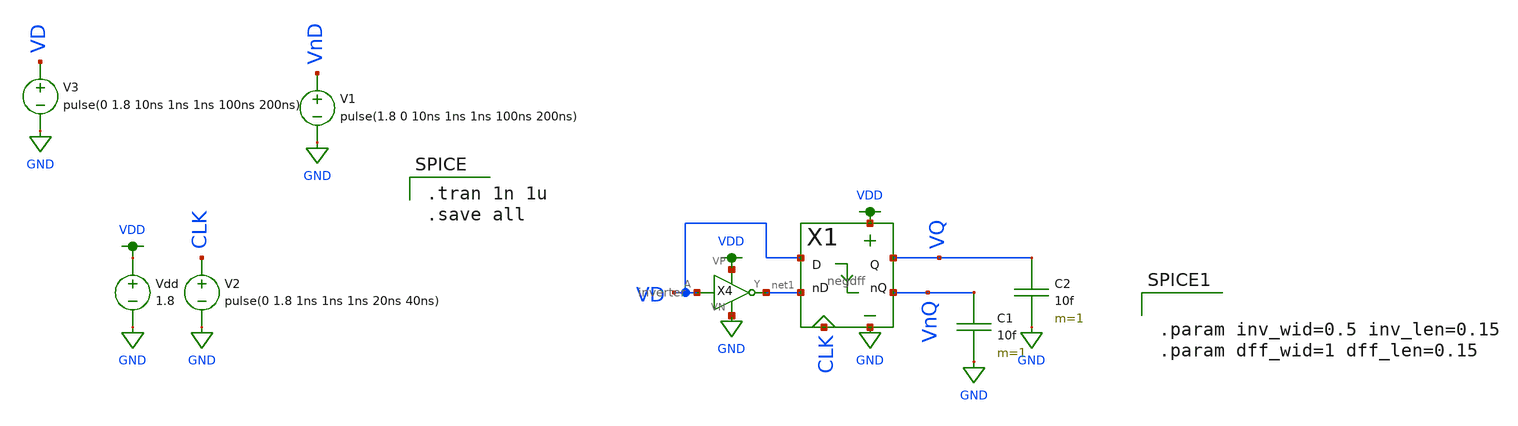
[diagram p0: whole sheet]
** sch_path: test_dff_tt2.sch
**.subckt test_dff_tt2
Vdd VDD GND 1.8
V2 CLK GND pulse(0 1.8 1ns 1ns 1ns 20ns 40ns)
V3 VD GND pulse(0 1.8 10ns 1ns 1ns 100ns 200ns)
V1 VnD GND pulse(1.8 0 10ns 1ns 1ns 100ns 200ns)
X4 VD net1 VDD GND inverter
C1 VnQ GND 10f m=1
C2 VQ GND 10f m=1
X1 GND VDD VnQ VQ CLK net1 VD negdff
**** begin user architecture code

.tran 1n 1u
.save all


.lib $::SKYWATER_MODELS/sky130.lib.spice tt



.param inv_wid=0.5 inv_len=0.15
.param dff_wid=1 dff_len=0.15


**** end user architecture code
**.ends

* expanding   symbol:  inverter.sym # of pins=4
** sym_path: inverter.sym
** sch_path: inverter.sch
.subckt inverter A Y VP VN
*.iopin VP
*.ipin A
*.opin Y
*.iopin VN
XM2 Y A VP VP sky130_fd_pr__pfet_01v8 L={inv_len} W={inv_wid} nf=1 ad='int((nf+1)/2) * W/nf * 0.29' as='int((nf+2)/2) * W/nf * 0.29'
+ pd='2*int((nf+1)/2) * (W/nf + 0.29)' ps='2*int((nf+2)/2) * (W/nf + 0.29)' nrd='0.29 / W' nrs='0.29 / W'
+ sa=0 sb=0 sd=0 mult=1 m=1
XM1 Y A VN VN sky130_fd_pr__nfet_01v8 L={inv_len} W={inv_wid} nf=1 ad='int((nf+1)/2) * W/nf * 0.29' as='int((nf+2)/2) * W/nf * 0.29'
+ pd='2*int((nf+1)/2) * (W/nf + 0.29)' ps='2*int((nf+2)/2) * (W/nf + 0.29)' nrd='0.29 / W' nrs='0.29 / W'
+ sa=0 sb=0 sd=0 mult=1 m=1
.ends


* expanding   symbol:  negdff.sym # of pins=7
** sym_path: negdff.sym
** sch_path: negdff.sch
.subckt negdff VN VP nQ Q PHI nD D
*.iopin VP
*.ipin D
*.opin Q
*.ipin nD
*.ipin PHI
*.opin nQ
*.iopin VN
X1 VN VP nQI QI PHI nD D n_csrl_latch
X2 VN VP nQ Q PHI nQI QI csrl_latch
.ends


* expanding   symbol:  n_csrl_latch.sym # of pins=7
** sym_path: n_csrl_latch.sym
** sch_path: n_csrl_latch.sch
.subckt n_csrl_latch VN VP nQ Q PHI nD D
*.ipin D
*.ipin nD
*.opin nQ
*.opin Q
*.ipin PHI
*.iopin VP
*.iopin VN
XM1 VN nD net3 VN sky130_fd_pr__nfet_01v8 L={dff_len} W={dff_wid} nf=1 ad='int((nf+1)/2) * W/nf * 0.29'
+ as='int((nf+2)/2) * W/nf * 0.29' pd='2*int((nf+1)/2) * (W/nf + 0.29)' ps='2*int((nf+2)/2) * (W/nf + 0.29)'
+ nrd='0.29 / W' nrs='0.29 / W' sa=0 sb=0 sd=0 mult=1 m=1
XM2 net3 PHI Q VN sky130_fd_pr__nfet_01v8 L={dff_len} W={dff_wid} nf=1 ad='int((nf+1)/2) * W/nf * 0.29'
+ as='int((nf+2)/2) * W/nf * 0.29' pd='2*int((nf+1)/2) * (W/nf + 0.29)' ps='2*int((nf+2)/2) * (W/nf + 0.29)'
+ nrd='0.29 / W' nrs='0.29 / W' sa=0 sb=0 sd=0 mult=1 m=1
XM3 VN nQ Q VN sky130_fd_pr__nfet_01v8 L={dff_len} W={dff_wid} nf=1 ad='int((nf+1)/2) * W/nf * 0.29'
+ as='int((nf+2)/2) * W/nf * 0.29' pd='2*int((nf+1)/2) * (W/nf + 0.29)' ps='2*int((nf+2)/2) * (W/nf + 0.29)'
+ nrd='0.29 / W' nrs='0.29 / W' sa=0 sb=0 sd=0 mult=1 m=1
XM4 net1 D VN VN sky130_fd_pr__nfet_01v8 L={dff_len} W={dff_wid} nf=1 ad='int((nf+1)/2) * W/nf * 0.29'
+ as='int((nf+2)/2) * W/nf * 0.29' pd='2*int((nf+1)/2) * (W/nf + 0.29)' ps='2*int((nf+2)/2) * (W/nf + 0.29)'
+ nrd='0.29 / W' nrs='0.29 / W' sa=0 sb=0 sd=0 mult=1 m=1
XM5 net1 PHI nQ VN sky130_fd_pr__nfet_01v8 L={dff_len} W={dff_wid} nf=1 ad='int((nf+1)/2) * W/nf * 0.29'
+ as='int((nf+2)/2) * W/nf * 0.29' pd='2*int((nf+1)/2) * (W/nf + 0.29)' ps='2*int((nf+2)/2) * (W/nf + 0.29)'
+ nrd='0.29 / W' nrs='0.29 / W' sa=0 sb=0 sd=0 mult=1 m=1
XM6 VN Q nQ VN sky130_fd_pr__nfet_01v8 L={dff_len} W={dff_wid} nf=1 ad='int((nf+1)/2) * W/nf * 0.29'
+ as='int((nf+2)/2) * W/nf * 0.29' pd='2*int((nf+1)/2) * (W/nf + 0.29)' ps='2*int((nf+2)/2) * (W/nf + 0.29)'
+ nrd='0.29 / W' nrs='0.29 / W' sa=0 sb=0 sd=0 mult=1 m=1
XM13 VP D net2 VP sky130_fd_pr__pfet_01v8 L={dff_len} W={dff_wid} nf=1 ad='int((nf+1)/2) * W/nf * 0.29'
+ as='int((nf+2)/2) * W/nf * 0.29' pd='2*int((nf+1)/2) * (W/nf + 0.29)' ps='2*int((nf+2)/2) * (W/nf + 0.29)'
+ nrd='0.29 / W' nrs='0.29 / W' sa=0 sb=0 sd=0 mult=1 m=1
XM14 net2 PHI VP VP sky130_fd_pr__pfet_01v8 L={dff_len} W={dff_wid} nf=1 ad='int((nf+1)/2) * W/nf * 0.29'
+ as='int((nf+2)/2) * W/nf * 0.29' pd='2*int((nf+1)/2) * (W/nf + 0.29)' ps='2*int((nf+2)/2) * (W/nf + 0.29)'
+ nrd='0.29 / W' nrs='0.29 / W' sa=0 sb=0 sd=0 mult=1 m=1
XM15 nQ Q net2 VP sky130_fd_pr__pfet_01v8 L={dff_len} W={dff_wid} nf=1 ad='int((nf+1)/2) * W/nf * 0.29'
+ as='int((nf+2)/2) * W/nf * 0.29' pd='2*int((nf+1)/2) * (W/nf + 0.29)' ps='2*int((nf+2)/2) * (W/nf + 0.29)'
+ nrd='0.29 / W' nrs='0.29 / W' sa=0 sb=0 sd=0 mult=1 m=1
XM16 net4 nD VP VP sky130_fd_pr__pfet_01v8 L={dff_len} W={dff_wid} nf=1 ad='int((nf+1)/2) * W/nf * 0.29'
+ as='int((nf+2)/2) * W/nf * 0.29' pd='2*int((nf+1)/2) * (W/nf + 0.29)' ps='2*int((nf+2)/2) * (W/nf + 0.29)'
+ nrd='0.29 / W' nrs='0.29 / W' sa=0 sb=0 sd=0 mult=1 m=1
XM17 net4 PHI VP VP sky130_fd_pr__pfet_01v8 L={dff_len} W={dff_wid} nf=1 ad='int((nf+1)/2) * W/nf * 0.29'
+ as='int((nf+2)/2) * W/nf * 0.29' pd='2*int((nf+1)/2) * (W/nf + 0.29)' ps='2*int((nf+2)/2) * (W/nf + 0.29)'
+ nrd='0.29 / W' nrs='0.29 / W' sa=0 sb=0 sd=0 mult=1 m=1
XM18 Q nQ net4 VP sky130_fd_pr__pfet_01v8 L={dff_len} W={dff_wid} nf=1 ad='int((nf+1)/2) * W/nf * 0.29'
+ as='int((nf+2)/2) * W/nf * 0.29' pd='2*int((nf+1)/2) * (W/nf + 0.29)' ps='2*int((nf+2)/2) * (W/nf + 0.29)'
+ nrd='0.29 / W' nrs='0.29 / W' sa=0 sb=0 sd=0 mult=1 m=1
.ends


* expanding   symbol:  csrl_latch.sym # of pins=7
** sym_path: csrl_latch.sym
** sch_path: csrl_latch.sch
.subckt csrl_latch VN VP nQ Q PHI nD D
*.ipin nD
*.ipin D
*.opin Q
*.opin nQ
*.ipin PHI
*.iopin VP
*.iopin VN
XM7 net3 D VN VN sky130_fd_pr__nfet_01v8 L={dff_len} W={dff_wid} nf=1 ad='int((nf+1)/2) * W/nf * 0.29'
+ as='int((nf+2)/2) * W/nf * 0.29' pd='2*int((nf+1)/2) * (W/nf + 0.29)' ps='2*int((nf+2)/2) * (W/nf + 0.29)'
+ nrd='0.29 / W' nrs='0.29 / W' sa=0 sb=0 sd=0 mult=1 m=1
XM8 VN PHI net3 VN sky130_fd_pr__nfet_01v8 L={dff_len} W={dff_wid} nf=1 ad='int((nf+1)/2) * W/nf * 0.29'
+ as='int((nf+2)/2) * W/nf * 0.29' pd='2*int((nf+1)/2) * (W/nf + 0.29)' ps='2*int((nf+2)/2) * (W/nf + 0.29)'
+ nrd='0.29 / W' nrs='0.29 / W' sa=0 sb=0 sd=0 mult=1 m=1
XM9 nQ Q net3 VN sky130_fd_pr__nfet_01v8 L={dff_len} W={dff_wid} nf=1 ad='int((nf+1)/2) * W/nf * 0.29'
+ as='int((nf+2)/2) * W/nf * 0.29' pd='2*int((nf+1)/2) * (W/nf + 0.29)' ps='2*int((nf+2)/2) * (W/nf + 0.29)'
+ nrd='0.29 / W' nrs='0.29 / W' sa=0 sb=0 sd=0 mult=1 m=1
XM10 VN nD net2 VN sky130_fd_pr__nfet_01v8 L={dff_len} W={dff_wid} nf=1 ad='int((nf+1)/2) * W/nf * 0.29'
+ as='int((nf+2)/2) * W/nf * 0.29' pd='2*int((nf+1)/2) * (W/nf + 0.29)' ps='2*int((nf+2)/2) * (W/nf + 0.29)'
+ nrd='0.29 / W' nrs='0.29 / W' sa=0 sb=0 sd=0 mult=1 m=1
XM11 VN PHI net2 VN sky130_fd_pr__nfet_01v8 L={dff_len} W={dff_wid} nf=1 ad='int((nf+1)/2) * W/nf * 0.29'
+ as='int((nf+2)/2) * W/nf * 0.29' pd='2*int((nf+1)/2) * (W/nf + 0.29)' ps='2*int((nf+2)/2) * (W/nf + 0.29)'
+ nrd='0.29 / W' nrs='0.29 / W' sa=0 sb=0 sd=0 mult=1 m=1
XM12 Q nQ net2 VN sky130_fd_pr__nfet_01v8 L={dff_len} W={dff_wid} nf=1 ad='int((nf+1)/2) * W/nf * 0.29'
+ as='int((nf+2)/2) * W/nf * 0.29' pd='2*int((nf+1)/2) * (W/nf + 0.29)' ps='2*int((nf+2)/2) * (W/nf + 0.29)'
+ nrd='0.29 / W' nrs='0.29 / W' sa=0 sb=0 sd=0 mult=1 m=1
XM19 net1 nD VP VP sky130_fd_pr__pfet_01v8 L={dff_len} W={dff_wid} nf=1 ad='int((nf+1)/2) * W/nf * 0.29'
+ as='int((nf+2)/2) * W/nf * 0.29' pd='2*int((nf+1)/2) * (W/nf + 0.29)' ps='2*int((nf+2)/2) * (W/nf + 0.29)'
+ nrd='0.29 / W' nrs='0.29 / W' sa=0 sb=0 sd=0 mult=1 m=1
XM20 Q PHI net1 VP sky130_fd_pr__pfet_01v8 L={dff_len} W={dff_wid} nf=1 ad='int((nf+1)/2) * W/nf * 0.29'
+ as='int((nf+2)/2) * W/nf * 0.29' pd='2*int((nf+1)/2) * (W/nf + 0.29)' ps='2*int((nf+2)/2) * (W/nf + 0.29)'
+ nrd='0.29 / W' nrs='0.29 / W' sa=0 sb=0 sd=0 mult=1 m=1
XM21 VP nQ Q VP sky130_fd_pr__pfet_01v8 L={dff_len} W={dff_wid} nf=1 ad='int((nf+1)/2) * W/nf * 0.29'
+ as='int((nf+2)/2) * W/nf * 0.29' pd='2*int((nf+1)/2) * (W/nf + 0.29)' ps='2*int((nf+2)/2) * (W/nf + 0.29)'
+ nrd='0.29 / W' nrs='0.29 / W' sa=0 sb=0 sd=0 mult=1 m=1
XM22 VP D net4 VP sky130_fd_pr__pfet_01v8 L={dff_len} W={dff_wid} nf=1 ad='int((nf+1)/2) * W/nf * 0.29'
+ as='int((nf+2)/2) * W/nf * 0.29' pd='2*int((nf+1)/2) * (W/nf + 0.29)' ps='2*int((nf+2)/2) * (W/nf + 0.29)'
+ nrd='0.29 / W' nrs='0.29 / W' sa=0 sb=0 sd=0 mult=1 m=1
XM23 nQ PHI net4 VP sky130_fd_pr__pfet_01v8 L={dff_len} W={dff_wid} nf=1 ad='int((nf+1)/2) * W/nf * 0.29'
+ as='int((nf+2)/2) * W/nf * 0.29' pd='2*int((nf+1)/2) * (W/nf + 0.29)' ps='2*int((nf+2)/2) * (W/nf + 0.29)'
+ nrd='0.29 / W' nrs='0.29 / W' sa=0 sb=0 sd=0 mult=1 m=1
XM24 VP Q nQ VP sky130_fd_pr__pfet_01v8 L={dff_len} W={dff_wid} nf=1 ad='int((nf+1)/2) * W/nf * 0.29'
+ as='int((nf+2)/2) * W/nf * 0.29' pd='2*int((nf+1)/2) * (W/nf + 0.29)' ps='2*int((nf+2)/2) * (W/nf + 0.29)'
+ nrd='0.29 / W' nrs='0.29 / W' sa=0 sb=0 sd=0 mult=1 m=1
.ends

.GLOBAL GND
.GLOBAL VDD
.end
